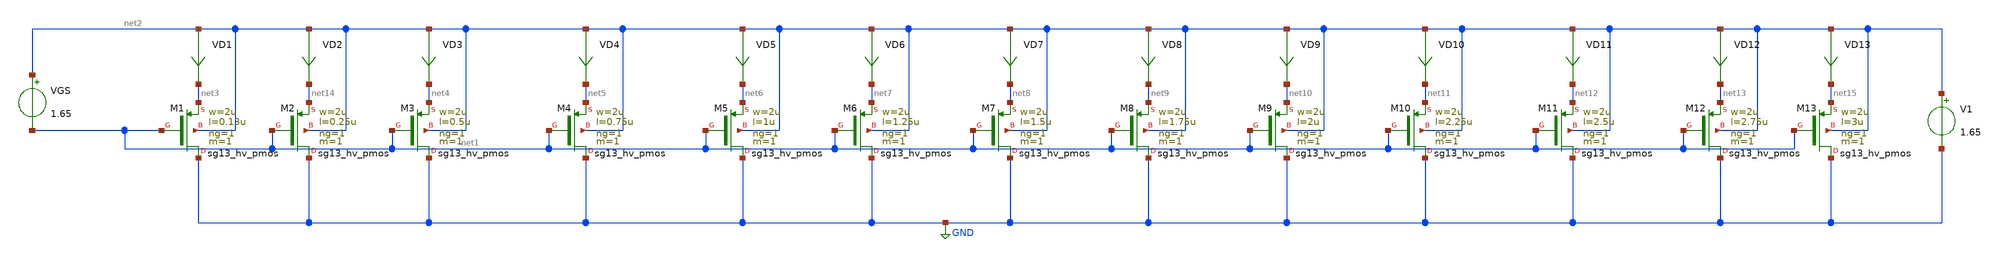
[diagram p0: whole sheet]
** sch_path: Design-Files/gmid_pmos_sg13_hv_pmos_tb.sch
**.subckt gmid_pmos_sg13_hv_pmos_tb
V1 net2 GND 1.65
VGS net2 net1 1.65
VD1 net2 net3 0
.save i(vd1)
VD2 net2 net14 0
.save i(vd2)
VD3 net2 net4 0
.save i(vd3)
VD4 net2 net5 0
.save i(vd4)
VD5 net2 net6 0
.save i(vd5)
VD6 net2 net7 0
.save i(vd6)
VD7 net2 net8 0
.save i(vd7)
VD8 net2 net9 0
.save i(vd8)
VD9 net2 net10 0
.save i(vd9)
VD10 net2 net11 0
.save i(vd10)
VD11 net2 net12 0
.save i(vd11)
VD12 net2 net13 0
.save i(vd12)
VD13 net2 net15 0
.save i(vd13)
XM1 GND net1 net3 net2 sg13_hv_pmos w=2u l=0.13u ng=1 m=1 mm_ok=1
XM2 GND net1 net14 net2 sg13_hv_pmos w=2u l=0.25u ng=1 m=1 mm_ok=1
XM3 GND net1 net4 net2 sg13_hv_pmos w=2u l=0.5u ng=1 m=1 mm_ok=1
XM4 GND net1 net5 net2 sg13_hv_pmos w=2u l=0.75u ng=1 m=1 mm_ok=1
XM5 GND net1 net6 net2 sg13_hv_pmos w=2u l=1u ng=1 m=1 mm_ok=1
XM6 GND net1 net7 net2 sg13_hv_pmos w=2u l=1.25u ng=1 m=1 mm_ok=1
XM7 GND net1 net8 net2 sg13_hv_pmos w=2u l=1.5u ng=1 m=1 mm_ok=1
XM8 GND net1 net9 net2 sg13_hv_pmos w=2u l=1.75u ng=1 m=1 mm_ok=1
XM9 GND net1 net10 net2 sg13_hv_pmos w=2u l=2u ng=1 m=1 mm_ok=1
XM10 GND net1 net11 net2 sg13_hv_pmos w=2u l=2.25u ng=1 m=1 mm_ok=1
XM11 GND net1 net12 net2 sg13_hv_pmos w=2u l=2.5u ng=1 m=1 mm_ok=1
XM12 GND net1 net13 net2 sg13_hv_pmos w=2u l=2.75u ng=1 m=1 mm_ok=1
XM13 GND net1 net15 net2 sg13_hv_pmos w=2u l=3u ng=1 m=1 mm_ok=1
**** begin user architecture code


.save @n.xm1.nsg13_hv_pmos[gm]
.save @n.xm1.nsg13_hv_pmos[id]
.save @n.xm1.nsg13_hv_pmos[vth]
.save @n.xm1.nsg13_hv_pmos[gds]
.save @n.xm1.nsg13_hv_pmos[cgg]
.save @n.xm1.nsg13_hv_pmos[cgs]
.save @n.xm1.nsg13_hv_pmos[cgd]
.save @n.xm2.nsg13_hv_pmos[gm]
.save @n.xm2.nsg13_hv_pmos[id]
.save @n.xm2.nsg13_hv_pmos[vth]
.save @n.xm2.nsg13_hv_pmos[gds]
.save @n.xm2.nsg13_hv_pmos[cgg]
.save @n.xm2.nsg13_hv_pmos[cgs]
.save @n.xm2.nsg13_hv_pmos[cgd]
.save @n.xm3.nsg13_hv_pmos[gm]
.save @n.xm3.nsg13_hv_pmos[id]
.save @n.xm3.nsg13_hv_pmos[vth]
.save @n.xm3.nsg13_hv_pmos[gds]
.save @n.xm3.nsg13_hv_pmos[cgg]
.save @n.xm3.nsg13_hv_pmos[cgs]
.save @n.xm3.nsg13_hv_pmos[cgd]
.save @n.xm4.nsg13_hv_pmos[gm]
.save @n.xm4.nsg13_hv_pmos[id]
.save @n.xm4.nsg13_hv_pmos[vth]
.save @n.xm4.nsg13_hv_pmos[gds]
.save @n.xm4.nsg13_hv_pmos[cgg]
.save @n.xm4.nsg13_hv_pmos[cgs]
.save @n.xm4.nsg13_hv_pmos[cgd]
.save @n.xm5.nsg13_hv_pmos[gm]
.save @n.xm5.nsg13_hv_pmos[id]
.save @n.xm5.nsg13_hv_pmos[vth]
.save @n.xm5.nsg13_hv_pmos[gds]
.save @n.xm5.nsg13_hv_pmos[cgg]
.save @n.xm5.nsg13_hv_pmos[cgs]
.save @n.xm5.nsg13_hv_pmos[cgd]
.save @n.xm6.nsg13_hv_pmos[gm]
.save @n.xm6.nsg13_hv_pmos[id]
.save @n.xm6.nsg13_hv_pmos[vth]
.save @n.xm6.nsg13_hv_pmos[gds]
.save @n.xm6.nsg13_hv_pmos[cgg]
.save @n.xm6.nsg13_hv_pmos[cgs]
.save @n.xm6.nsg13_hv_pmos[cgd]
.save @n.xm7.nsg13_hv_pmos[gm]
.save @n.xm7.nsg13_hv_pmos[id]
.save @n.xm7.nsg13_hv_pmos[vth]
.save @n.xm7.nsg13_hv_pmos[gds]
.save @n.xm7.nsg13_hv_pmos[cgg]
.save @n.xm7.nsg13_hv_pmos[cgs]
.save @n.xm7.nsg13_hv_pmos[cgd]
.save @n.xm7.nsg13_hv_pmos[gm]
.save @n.xm7.nsg13_hv_pmos[id]
.save @n.xm7.nsg13_hv_pmos[vth]
.save @n.xm7.nsg13_hv_pmos[gds]
.save @n.xm7.nsg13_hv_pmos[cgg]
.save @n.xm7.nsg13_hv_pmos[cgs]
.save @n.xm7.nsg13_hv_pmos[cgd]
.save @n.xm8.nsg13_hv_pmos[gm]
.save @n.xm8.nsg13_hv_pmos[id]
.save @n.xm8.nsg13_hv_pmos[vth]
.save @n.xm8.nsg13_hv_pmos[gds]
.save @n.xm8.nsg13_hv_pmos[cgg]
.save @n.xm8.nsg13_hv_pmos[cgs]
.save @n.xm8.nsg13_hv_pmos[cgd]
.save @n.xm9.nsg13_hv_pmos[gm]
.save @n.xm9.nsg13_hv_pmos[id]
.save @n.xm9.nsg13_hv_pmos[vth]
.save @n.xm9.nsg13_hv_pmos[gds]
.save @n.xm9.nsg13_hv_pmos[cgg]
.save @n.xm9.nsg13_hv_pmos[cgs]
.save @n.xm9.nsg13_hv_pmos[cgd]
.save @n.xm10.nsg13_hv_pmos[gm]
.save @n.xm10.nsg13_hv_pmos[id]
.save @n.xm10.nsg13_hv_pmos[vth]
.save @n.xm10.nsg13_hv_pmos[gds]
.save @n.xm10.nsg13_hv_pmos[cgg]
.save @n.xm10.nsg13_hv_pmos[cgs]
.save @n.xm10.nsg13_hv_pmos[cgd]
.save @n.xm11.nsg13_hv_pmos[gm]
.save @n.xm11.nsg13_hv_pmos[id]
.save @n.xm11.nsg13_hv_pmos[vth]
.save @n.xm11.nsg13_hv_pmos[gds]
.save @n.xm11.nsg13_hv_pmos[cgg]
.save @n.xm11.nsg13_hv_pmos[cgs]
.save @n.xm11.nsg13_hv_pmos[cgd]
.save @n.xm12.nsg13_hv_pmos[gm]
.save @n.xm12.nsg13_hv_pmos[id]
.save @n.xm12.nsg13_hv_pmos[vth]
.save @n.xm12.nsg13_hv_pmos[gds]
.save @n.xm12.nsg13_hv_pmos[cgg]
.save @n.xm12.nsg13_hv_pmos[cgs]
.save @n.xm12.nsg13_hv_pmos[cgd]
.save @n.xm13.nsg13_hv_pmos[gm]
.save @n.xm13.nsg13_hv_pmos[id]
.save @n.xm13.nsg13_hv_pmos[vth]
.save @n.xm13.nsg13_hv_pmos[gds]
.save @n.xm13.nsg13_hv_pmos[cgg]
.save @n.xm13.nsg13_hv_pmos[cgs]
.save @n.xm13.nsg13_hv_pmos[cgd]




.option wnflag=1
.option savecurrents
.temp 27
.control
save all
dc VGS 0.01 3.3 0.1m
remzerovec
write /foss/designs/IHP130_Designs/PDK_CHAR/HV_PMOS/gmid_pmos_sg13_hv_pmos_tb.raw

plot @n.xm1.nsg13_hv_pmos[gm]
plot @n.xm2.nsg13_hv_pmos[gm]
plot @n.xm3.nsg13_hv_pmos[gm]
plot @n.xm4.nsg13_hv_pmos[gm]
plot @n.xm5.nsg13_hv_pmos[gm]
plot @n.xm6.nsg13_hv_pmos[gm]
plot @n.xm7.nsg13_hv_pmos[gm]
plot @n.xm8.nsg13_hv_pmos[gm]
plot @n.xm9.nsg13_hv_pmos[gm]
plot @n.xm10.nsg13_hv_pmos[gm]
plot @n.xm11.nsg13_hv_pmos[gm]
plot @n.xm12.nsg13_hv_pmos[gm]
plot @n.xm13.nsg13_hv_pmos[gm]

wrdata /foss/designs/IHP130_Designs/PDK_CHAR/HV_PMOS/gmid_pmos_1_sg13_hv_pmos_tb.txt
+ @n.xm1.nsg13_hv_pmos[gm] i(VD1) @n.xm1.nsg13_hv_pmos[vth] @n.xm1.nsg13_hv_pmos[gds] @n.xm1.nsg13_hv_pmos[cgg]
+ @n.xm1.nsg13_hv_pmos[cgs] @n.xm1.nsg13_hv_pmos[cgd]
wrdata /foss/designs/IHP130_Designs/PDK_CHAR/HV_PMOS/gmid_pmos_2_sg13_hv_pmos_tb.txt
+ @n.xm2.nsg13_hv_pmos[gm] i(VD2) @n.xm2.nsg13_hv_pmos[vth] @n.xm2.nsg13_hv_pmos[gds] @n.xm2.nsg13_hv_pmos[cgg]
+ @n.xm2.nsg13_hv_pmos[cgs] @n.xm2.nsg13_hv_pmos[cgd]
wrdata /foss/designs/IHP130_Designs/PDK_CHAR/HV_PMOS/gmid_pmos_3_sg13_hv_pmos_tb.txt
+ @n.xm3.nsg13_hv_pmos[gm] i(VD3) @n.xm3.nsg13_hv_pmos[vth] @n.xm3.nsg13_hv_pmos[gds] @n.xm3.nsg13_hv_pmos[cgg]
+ @n.xm3.nsg13_hv_pmos[cgs] @n.xm3.nsg13_hv_pmos[cgd]
wrdata /foss/designs/IHP130_Designs/PDK_CHAR/HV_PMOS/gmid_pmos_4_sg13_hv_pmos_tb.txt
+ @n.xm4.nsg13_hv_pmos[gm] i(VD4) @n.xm4.nsg13_hv_pmos[vth] @n.xm4.nsg13_hv_pmos[gds] @n.xm4.nsg13_hv_pmos[cgg]
+ @n.xm4.nsg13_hv_pmos[cgs] @n.xm4.nsg13_hv_pmos[cgd]
wrdata /foss/designs/IHP130_Designs/PDK_CHAR/HV_PMOS/gmid_pmos_5_sg13_hv_pmos_tb.txt
+ @n.xm5.nsg13_hv_pmos[gm] i(VD5) @n.xm5.nsg13_hv_pmos[vth] @n.xm5.nsg13_hv_pmos[gds] @n.xm5.nsg13_hv_pmos[cgg]
+ @n.xm5.nsg13_hv_pmos[cgs] @n.xm5.nsg13_hv_pmos[cgd]
wrdata /foss/designs/IHP130_Designs/PDK_CHAR/HV_PMOS/gmid_pmos_6_sg13_hv_pmos_tb.txt
+ @n.xm6.nsg13_hv_pmos[gm] i(VD6) @n.xm6.nsg13_hv_pmos[vth] @n.xm6.nsg13_hv_pmos[gds] @n.xm6.nsg13_hv_pmos[cgg]
+ @n.xm6.nsg13_hv_pmos[cgs] @n.xm6.nsg13_hv_pmos[cgd]
wrdata /foss/designs/IHP130_Designs/PDK_CHAR/HV_PMOS/gmid_pmos_7_sg13_hv_pmos_tb.txt
+ @n.xm7.nsg13_hv_pmos[gm] i(VD7) @n.xm7.nsg13_hv_pmos[vth] @n.xm7.nsg13_hv_pmos[gds] @n.xm7.nsg13_hv_pmos[cgg]
+ @n.xm7.nsg13_hv_pmos[cgs] @n.xm7.nsg13_hv_pmos[cgd]
wrdata /foss/designs/IHP130_Designs/PDK_CHAR/HV_PMOS/gmid_pmos_8_sg13_hv_pmos_tb.txt
+ @n.xm8.nsg13_hv_pmos[gm] i(VD8) @n.xm8.nsg13_hv_pmos[vth] @n.xm8.nsg13_hv_pmos[gds] @n.xm8.nsg13_hv_pmos[cgg]
+ @n.xm8.nsg13_hv_pmos[cgs] @n.xm8.nsg13_hv_pmos[cgd]
wrdata /foss/designs/IHP130_Designs/PDK_CHAR/HV_PMOS/gmid_pmos_9_sg13_hv_pmos_tb.txt
+ @n.xm9.nsg13_hv_pmos[gm] i(VD9) @n.xm9.nsg13_hv_pmos[vth] @n.xm9.nsg13_hv_pmos[gds] @n.xm9.nsg13_hv_pmos[cgg]
+ @n.xm9.nsg13_hv_pmos[cgs] @n.xm9.nsg13_hv_pmos[cgd]
wrdata /foss/designs/IHP130_Designs/PDK_CHAR/HV_PMOS/gmid_pmos_10_sg13_hv_pmos_tb.txt
+ @n.xm10.nsg13_hv_pmos[gm] i(VD10) @n.xm10.nsg13_hv_pmos[vth] @n.xm10.nsg13_hv_pmos[gds] @n.xm10.nsg13_hv_pmos[cgg]
+ @n.xm10.nsg13_hv_pmos[cgs] @n.xm10.nsg13_hv_pmos[cgd]
wrdata /foss/designs/IHP130_Designs/PDK_CHAR/HV_PMOS/gmid_pmos_11_sg13_hv_pmos_tb.txt
+ @n.xm11.nsg13_hv_pmos[gm] i(VD11) @n.xm11.nsg13_hv_pmos[vth] @n.xm11.nsg13_hv_pmos[gds] @n.xm11.nsg13_hv_pmos[cgg]
+ @n.xm11.nsg13_hv_pmos[cgs] @n.xm11.nsg13_hv_pmos[cgd]
wrdata /foss/designs/IHP130_Designs/PDK_CHAR/HV_PMOS/gmid_pmos_12_sg13_hv_pmos_tb.txt
+ @n.xm12.nsg13_hv_pmos[gm] i(VD12) @n.xm12.nsg13_hv_pmos[vth] @n.xm12.nsg13_hv_pmos[gds] @n.xm12.nsg13_hv_pmos[cgg]
+ @n.xm12.nsg13_hv_pmos[cgs] @n.xm12.nsg13_hv_pmos[cgd]
wrdata /foss/designs/IHP130_Designs/PDK_CHAR/HV_PMOS/gmid_pmos_13_sg13_hv_pmos_tb.txt
+ @n.xm13.nsg13_hv_pmos[gm] i(VD13) @n.xm13.nsg13_hv_pmos[vth] @n.xm13.nsg13_hv_pmos[gds] @n.xm13.nsg13_hv_pmos[cgg]
+ @n.xm13.nsg13_hv_pmos[cgs] @n.xm13.nsg13_hv_pmos[cgd]

set appendwrite
op
remzerovec
write /foss/designs/IHP130_Designs/PDK_CHAR/HV_PMOS/gmid_pmos_sg13_hv_pmos_tb.raw
quit 0
.endc



.lib cornerMOShv.lib mos_tt

**** end user architecture code
**.ends
.GLOBAL GND
.end
